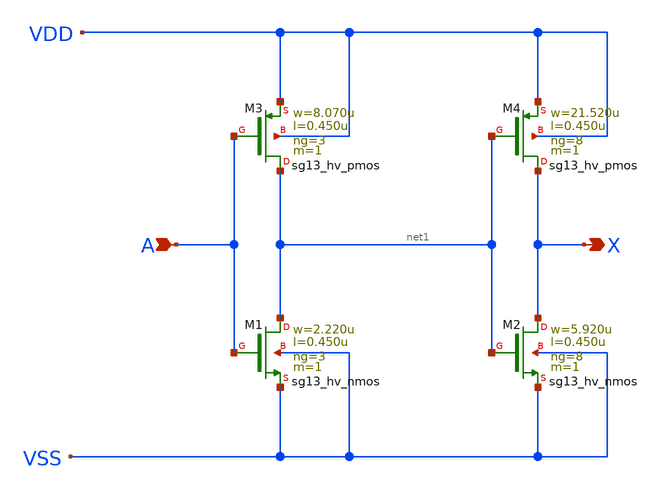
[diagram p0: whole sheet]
** sch_path: ihp-sg13g2/libs.ref/sg13g2_stdcell_hv/sch/xschem/sg13g2_hv_buf_8.sch
* Copyright 2023 IHP PDK Authors
* Licensed under the Apache License, Version 2.0 (the "License");
* you may not use this file except in compliance with the License.
* You may obtain a copy of the License at
* https://www.apache.org/licenses/LICENSE-2.0
* Unless required by applicable law or agreed to in writing, software
* distributed under the License is distributed on an "AS IS" BASIS,
* WITHOUT WARRANTIES OR CONDITIONS OF ANY KIND, either express or implied.
* See the License for the specific language governing permissions and
* limitations under the License.
**.subckt sg13g2_hv_buf_8 A X
*.ipin A
*.opin X
XM1 net1 A VSS VSS sg13_hv_nmos w=2.220u l=0.450u ng=3 m=1 mm_ok=1
XM2 X net1 VSS VSS sg13_hv_nmos w=5.920u l=0.450u ng=8 m=1 mm_ok=1
XM3 net1 A VDD VDD sg13_hv_pmos w=8.070u l=0.450u ng=3 m=1 mm_ok=1
XM4 X net1 VDD VDD sg13_hv_pmos w=21.520u l=0.450u ng=8 m=1 mm_ok=1
**.ends
.end
